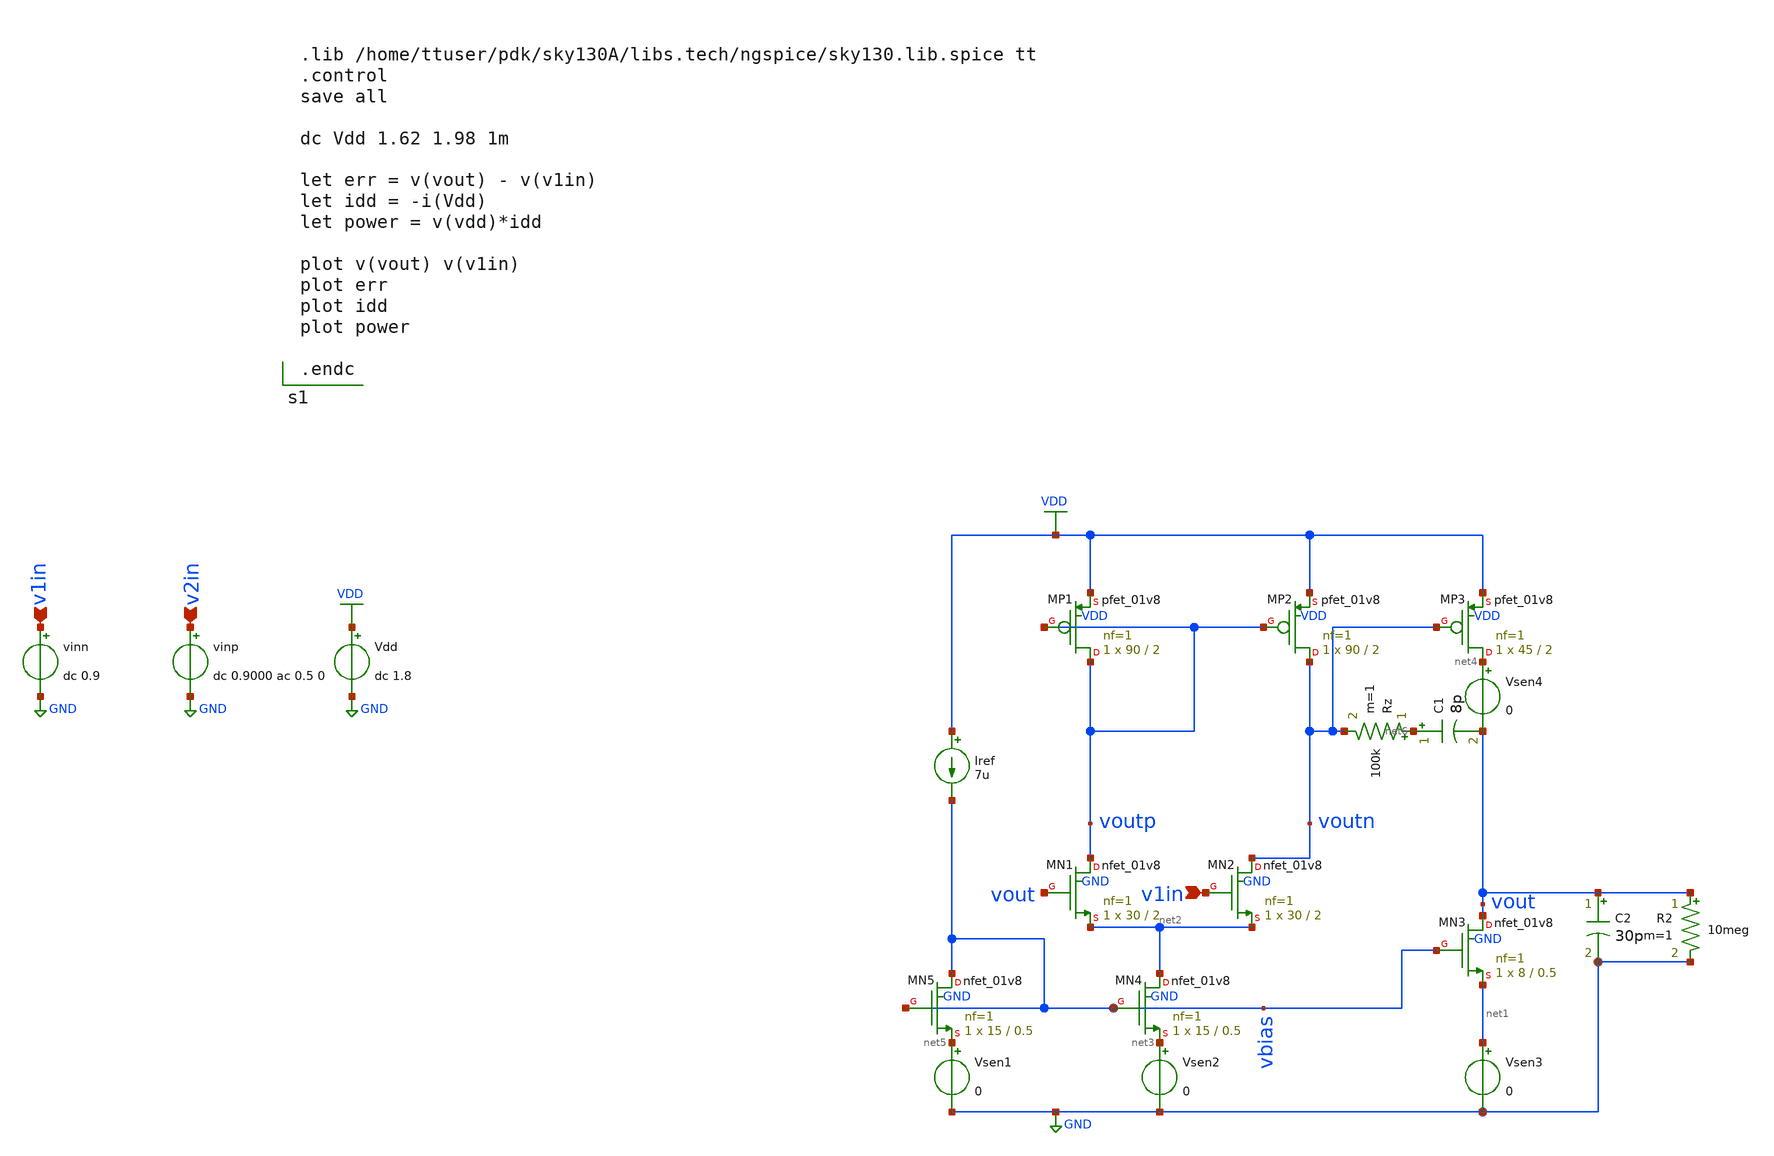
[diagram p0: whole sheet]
** sch_path: testbenches/prelayout/diffpairPVTVar.sch
**.subckt diffpairPVTVar v1in v1in v2in
*.ipin v1in
*.ipin v1in
*.ipin v2in
Vdd VDD GND dc 1.8
vinp v2in GND dc 0.9000 ac 0.5 0
vinn v1in GND dc 0.9
XMN1 voutp vout net2 GND sky130_fd_pr__nfet_01v8 L=2 W=30 nf=1 ad='int((nf+1)/2) * W/nf * 0.29' as='int((nf+2)/2) * W/nf * 0.29'
+ pd='2*int((nf+1)/2) * (W/nf + 0.29)' ps='2*int((nf+2)/2) * (W/nf + 0.29)' nrd='0.29 / W' nrs='0.29 / W'
+ sa=0 sb=0 sd=0 mult=1 m=1
XMN2 voutn v1in net2 GND sky130_fd_pr__nfet_01v8 L=2 W=30 nf=1 ad='int((nf+1)/2) * W/nf * 0.29' as='int((nf+2)/2) * W/nf * 0.29'
+ pd='2*int((nf+1)/2) * (W/nf + 0.29)' ps='2*int((nf+2)/2) * (W/nf + 0.29)' nrd='0.29 / W' nrs='0.29 / W'
+ sa=0 sb=0 sd=0 mult=1 m=1
XMP1 voutp voutp VDD VDD sky130_fd_pr__pfet_01v8 L=2 W=90 nf=1 ad='int((nf+1)/2) * W/nf * 0.29' as='int((nf+2)/2) * W/nf * 0.29'
+ pd='2*int((nf+1)/2) * (W/nf + 0.29)' ps='2*int((nf+2)/2) * (W/nf + 0.29)' nrd='0.29 / W' nrs='0.29 / W'
+ sa=0 sb=0 sd=0 mult=1 m=1
XMP2 voutn voutp VDD VDD sky130_fd_pr__pfet_01v8 L=2 W=90 nf=1 ad='int((nf+1)/2) * W/nf * 0.29' as='int((nf+2)/2) * W/nf * 0.29'
+ pd='2*int((nf+1)/2) * (W/nf + 0.29)' ps='2*int((nf+2)/2) * (W/nf + 0.29)' nrd='0.29 / W' nrs='0.29 / W'
+ sa=0 sb=0 sd=0 mult=1 m=1
Iref VDD vbias 7u
Vsen2 net3 GND 0
XMP3 net4 voutn VDD VDD sky130_fd_pr__pfet_01v8 L=2 W=45 nf=1 ad='int((nf+1)/2) * W/nf * 0.29' as='int((nf+2)/2) * W/nf * 0.29'
+ pd='2*int((nf+1)/2) * (W/nf + 0.29)' ps='2*int((nf+2)/2) * (W/nf + 0.29)' nrd='0.29 / W' nrs='0.29 / W'
+ sa=0 sb=0 sd=0 mult=1 m=1
XMN3 vout vbias net1 GND sky130_fd_pr__nfet_01v8 L=0.5 W=8 nf=1 ad='int((nf+1)/2) * W/nf * 0.29' as='int((nf+2)/2) * W/nf * 0.29'
+ pd='2*int((nf+1)/2) * (W/nf + 0.29)' ps='2*int((nf+2)/2) * (W/nf + 0.29)' nrd='0.29 / W' nrs='0.29 / W'
+ sa=0 sb=0 sd=0 mult=1 m=1
Vsen3 net1 GND 0
Vsen1 net5 GND 0
C1 net6 vout 8p m=1
XMN4 net2 vbias net3 GND sky130_fd_pr__nfet_01v8 L=0.5 W=15 nf=1 ad='int((nf+1)/2) * W/nf * 0.29' as='int((nf+2)/2) * W/nf * 0.29'
+ pd='2*int((nf+1)/2) * (W/nf + 0.29)' ps='2*int((nf+2)/2) * (W/nf + 0.29)' nrd='0.29 / W' nrs='0.29 / W'
+ sa=0 sb=0 sd=0 mult=1 m=1
XMN5 vbias vbias net5 GND sky130_fd_pr__nfet_01v8 L=0.5 W=15 nf=1 ad='int((nf+1)/2) * W/nf * 0.29' as='int((nf+2)/2) * W/nf * 0.29'
+ pd='2*int((nf+1)/2) * (W/nf + 0.29)' ps='2*int((nf+2)/2) * (W/nf + 0.29)' nrd='0.29 / W' nrs='0.29 / W'
+ sa=0 sb=0 sd=0 mult=1 m=1
C2 vout GND 30p m=1
Rz net6 voutn 100k m=1
Vsen4 net4 vout 0
R2 vout GND 10meg m=1
**** begin user architecture code


.lib /home/ttuser/pdk/sky130A/libs.tech/ngspice/sky130.lib.spice tt
.control
save all

dc Vdd 1.62 1.98 1m

let err = v(vout) - v(v1in)
let idd = -i(Vdd)
let power = v(vdd)*idd

plot v(vout) v(v1in)
plot err
plot idd
plot power

.endc


**** end user architecture code
**.ends
.GLOBAL VDD
.GLOBAL GND
.end
